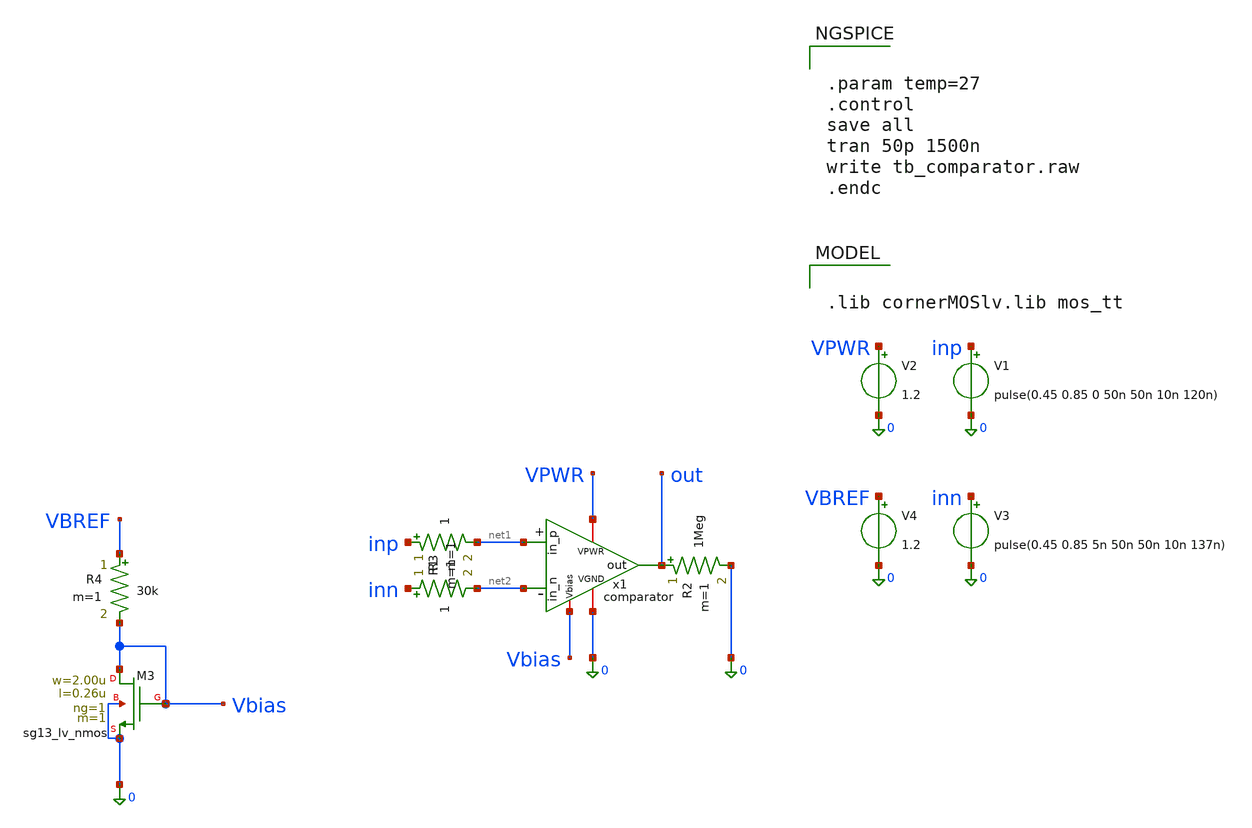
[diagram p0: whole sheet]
** sch_path: xschem/tb_comparator.sch
**.subckt tb_comparator
V1 inp 0 pulse(0.45 0.85 0 50n 50n 10n 120n)
R1 inp net1 1 m=1
R2 out 0 1Meg m=1
V2 VPWR 0 1.2
x1 VPWR 0 out net2 net1 Vbias comparator
R3 inn net2 1 m=1
V3 inn 0 pulse(0.45 0.85 5n 50n 50n 10n 137n)
XM3 Vbias Vbias 0 0 sg13_lv_nmos w=2.00u l=0.26u ng=1 m=1 mm_ok=1
V4 VBREF 0 1.2
R4 VBREF Vbias 30k m=1
**** begin user architecture code

.lib cornerMOSlv.lib mos_tt



.param temp=27
.control
save all
tran 50p 1500n
write tb_comparator.raw
.endc


**** end user architecture code
**.ends

* expanding   symbol:  comparator.sym # of pins=6
** sym_path: xschem/comparator.sym
** sch_path: xschem/comparator.sch
.subckt comparator VPWR VGND out in_n in_p Vbias
*.iopin VPWR
*.ipin in_p
*.ipin in_n
*.opin out
*.iopin VGND
*.ipin Vbias
XM1 net3 in_p net1 VGND sg13_lv_nmos w=4.00u l=0.26u ng=1 m=1 mm_ok=1
XM4 net2 net3 VPWR VPWR sg13_lv_pmos w=8.00u l=0.26u ng=1 m=1 mm_ok=1
XM5 net1 Vbias VGND VGND sg13_lv_nmos w=2.00u l=0.39u ng=1 m=1 mm_ok=1
XM2 net2 in_n net1 VGND sg13_lv_nmos w=4.00u l=0.26u ng=1 m=1 mm_ok=1
XM3 net3 net3 VPWR VPWR sg13_lv_pmos w=8.00u l=0.26u ng=1 m=1 mm_ok=1
XM6 net4 net2 VPWR VPWR sg13_lv_pmos w=8.00u l=0.26u ng=1 m=1 mm_ok=1
XM7 net4 Vbias VGND VGND sg13_lv_nmos w=2.00u l=0.39u ng=1 m=1 mm_ok=1
XM8 out net4 VPWR VPWR sg13_lv_pmos w=1.20u l=0.13u ng=1 m=1 mm_ok=1
XM9 out net4 VGND VGND sg13_lv_nmos w=0.50u l=0.13u ng=1 m=1 mm_ok=1
.ends

.end
